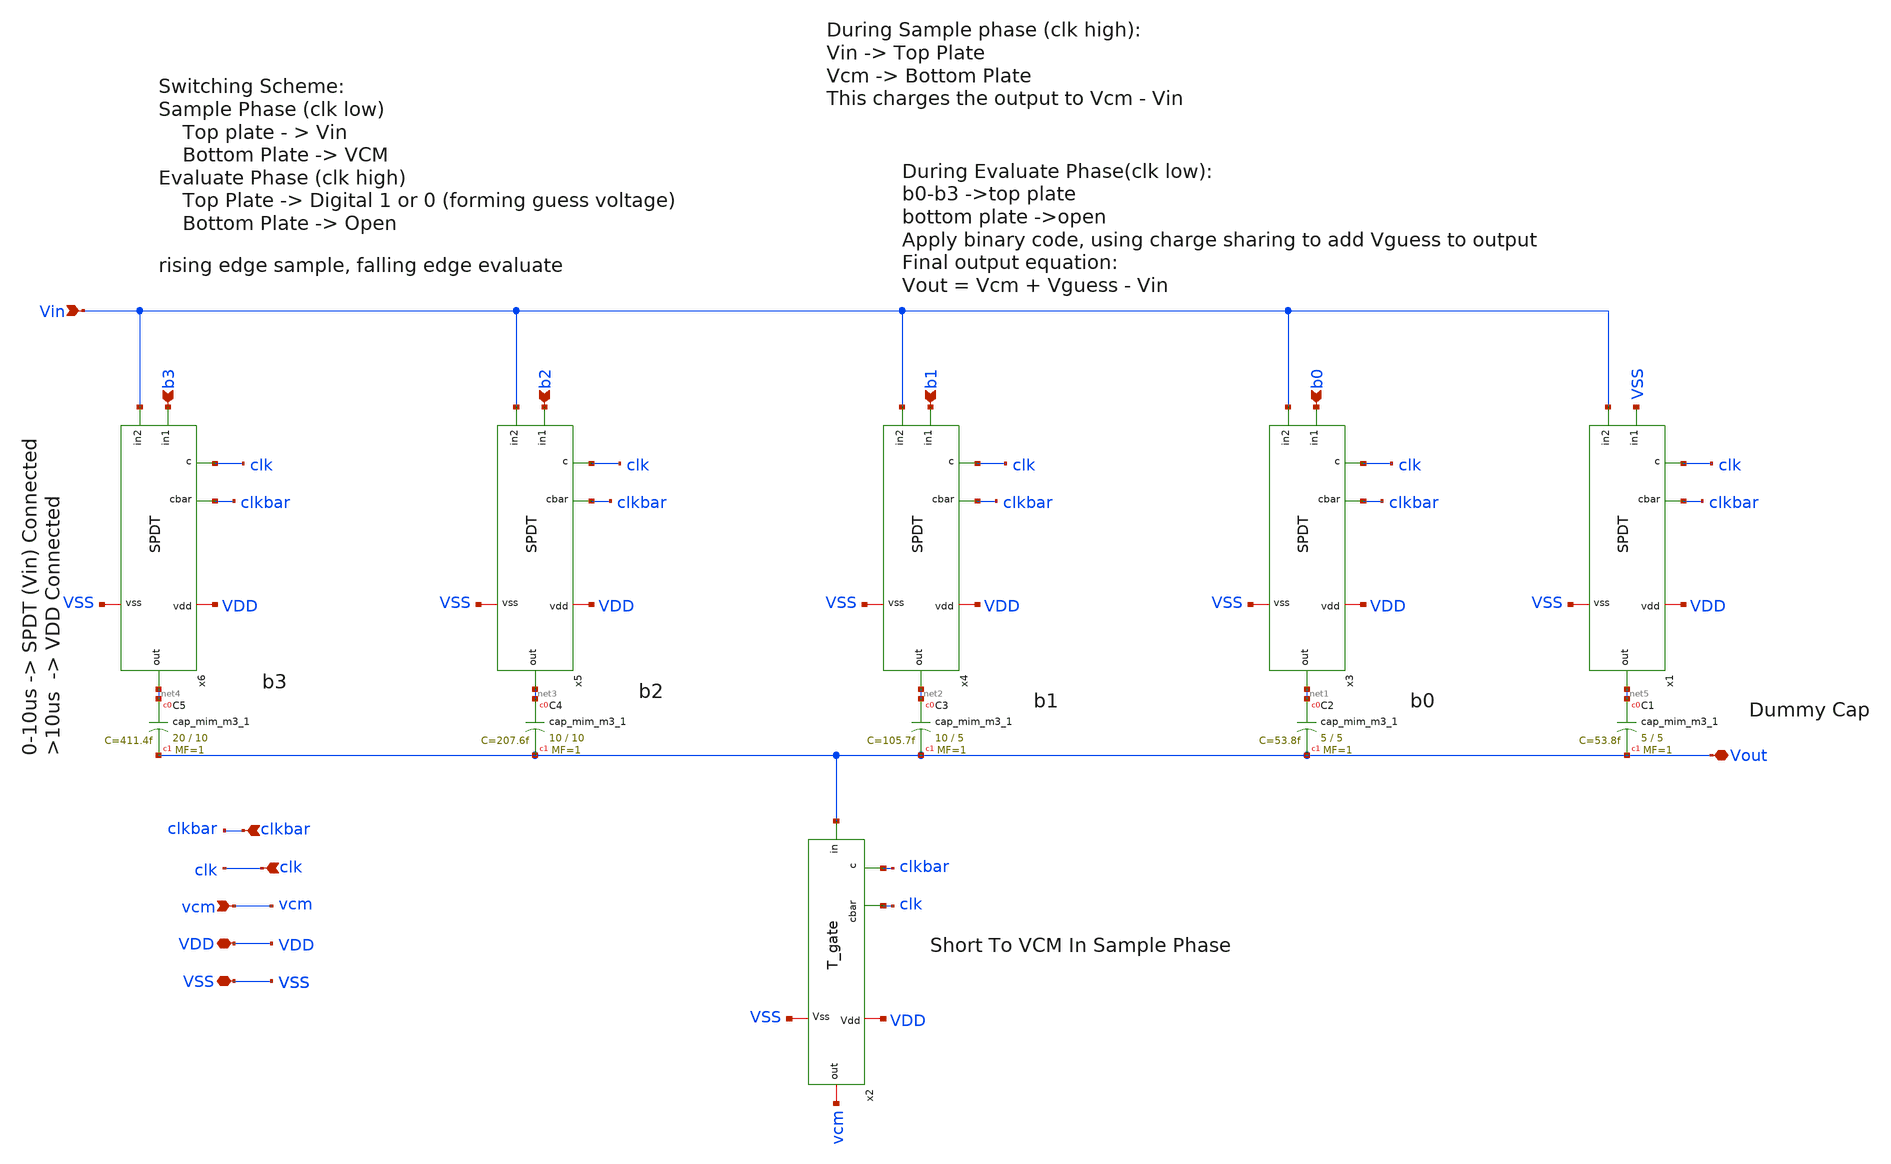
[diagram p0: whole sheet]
** sch_path: ADC/16bit_C2C/MagicAndSpice/CDAC_4bit_VCM_simplified.sch
**.subckt CDAC_4bit_VCM_simplified Vin clk clkbar vcm VDD b3 b2 b1 Vout b0 VSS
*.ipin Vin
*.ipin clk
*.ipin clkbar
*.ipin vcm
*.iopin VDD
*.ipin b3
*.ipin b2
*.ipin b1
*.iopin Vout
*.ipin b0
*.iopin VSS
XC1 net5 Vout sky130_fd_pr__cap_mim_m3_1 W=5 L=5 MF=1 m=1
XC2 net1 Vout sky130_fd_pr__cap_mim_m3_1 W=5 L=5 MF=1 m=1
x2 clkbar vcm Vout VDD clk VSS T_gate
x3 clkbar VDD VSS clk b0 net1 Vin SPDT
XC3 net2 Vout sky130_fd_pr__cap_mim_m3_1 W=10 L=5 MF=1 m=1
x4 clkbar VDD VSS clk b1 net2 Vin SPDT
XC4 net3 Vout sky130_fd_pr__cap_mim_m3_1 W=10 L=10 MF=1 m=1
x5 clkbar VDD VSS clk b2 net3 Vin SPDT
XC5 net4 Vout sky130_fd_pr__cap_mim_m3_1 W=20 L=10 MF=1 m=1
x6 clkbar VDD VSS clk b3 net4 Vin SPDT
x1 clkbar VDD VSS clk VSS net5 Vin SPDT
**.ends
.end
